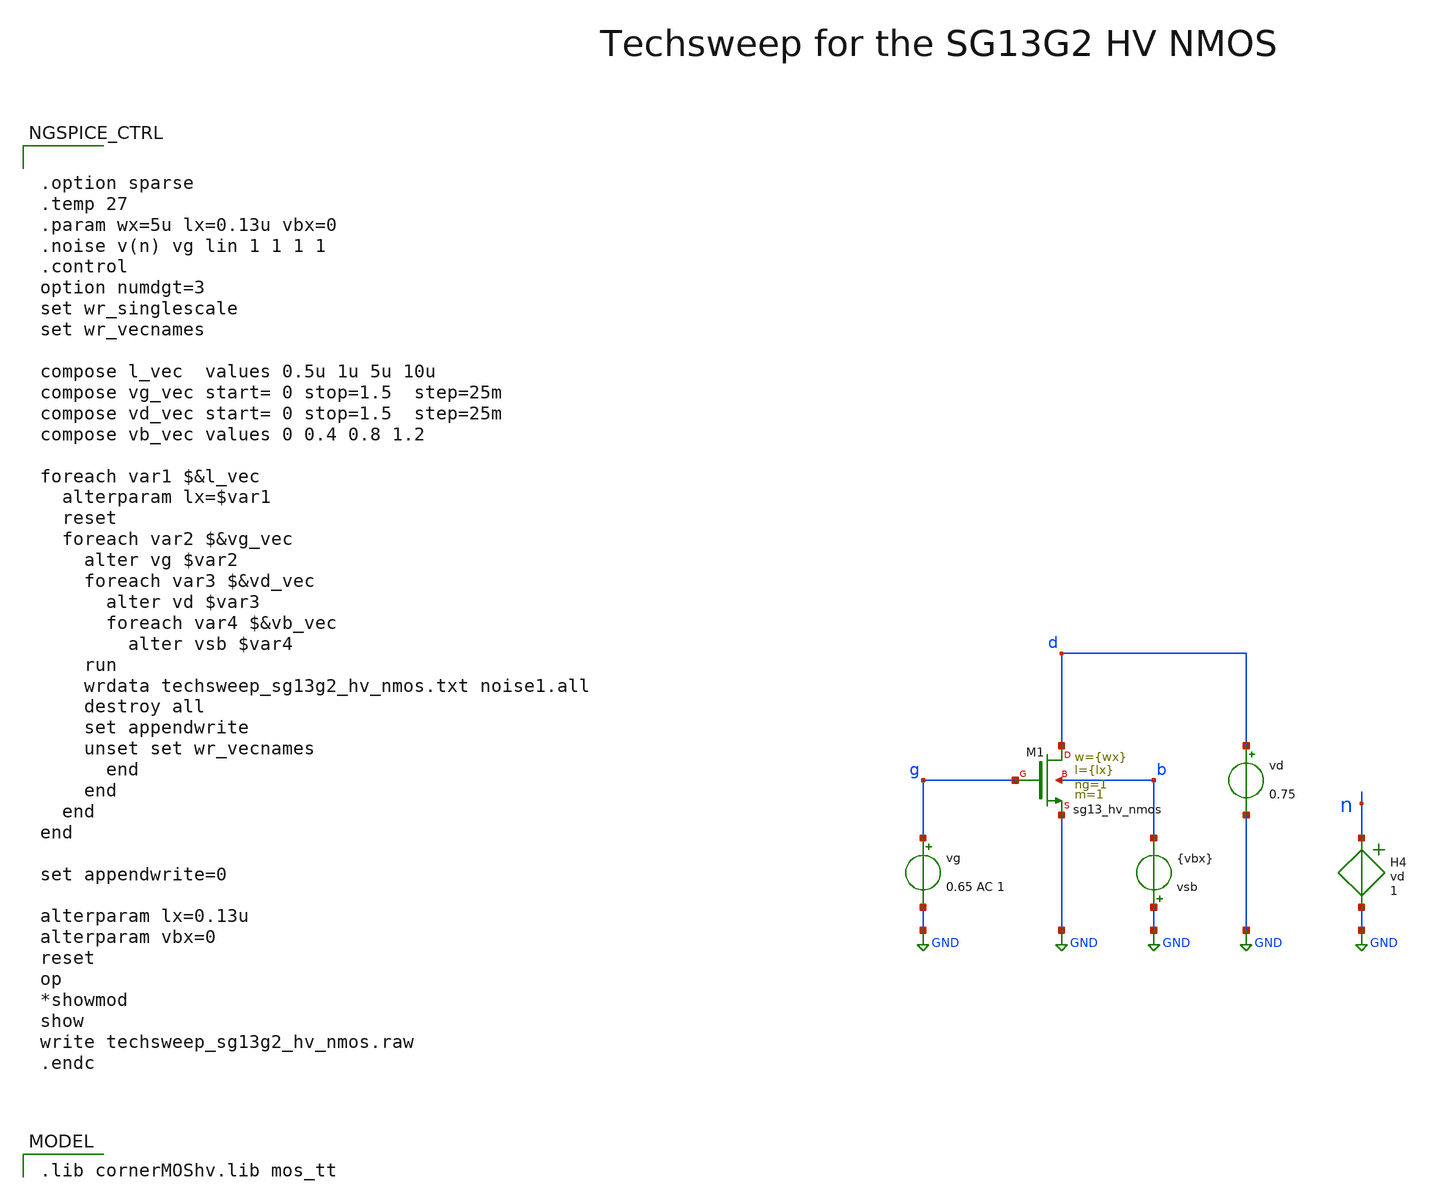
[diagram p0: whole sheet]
** sch_path: SG13G2_ATBS-ADC-main/xschem/techsweep/sg13g2_hv_nmos/techsweep_sg13g2_hv_nmos.sch
* (c) 2024 H. Pretl & S. Dorrer (adapted from B. Murmann)
**.subckt techsweep_sg13g2_hv_nmos
vg g GND 0.65 AC 1
vd d GND 0.75
vsb GND b {vbx}
H4 n GND vd 1
XM1 d g GND b sg13_hv_nmos w={wx} l={lx} ng=1 m=1 mm_ok=1
**** begin user architecture code
 .lib cornerMOShv.lib mos_tt



.option sparse
.temp 27
.param wx=5u lx=0.13u vbx=0
.noise v(n) vg lin 1 1 1 1
.control
option numdgt=3
set wr_singlescale
set wr_vecnames

compose l_vec  values 0.5u 1u 5u 10u
compose vg_vec start= 0 stop=1.5  step=25m
compose vd_vec start= 0 stop=1.5  step=25m
compose vb_vec values 0 0.4 0.8 1.2

foreach var1 $&l_vec
  alterparam lx=$var1
  reset
  foreach var2 $&vg_vec
    alter vg $var2
    foreach var3 $&vd_vec
      alter vd $var3
      foreach var4 $&vb_vec
        alter vsb $var4
	run
	wrdata techsweep_sg13g2_hv_nmos.txt noise1.all
	destroy all
	set appendwrite
	unset set wr_vecnames
      end
    end
  end
end

set appendwrite=0

alterparam lx=0.13u
alterparam vbx=0
reset
op
*showmod
show
write techsweep_sg13g2_hv_nmos.raw
.endc




.save b d g n
.save @n.xm1.nsg13_hv_nmos[cgsol]
.save @n.xm1.nsg13_hv_nmos[cgdol]
.save @n.xm1.nsg13_hv_nmos[cdd]
.save @n.xm1.nsg13_hv_nmos[cgb]
.save @n.xm1.nsg13_hv_nmos[cgd]
.save @n.xm1.nsg13_hv_nmos[cgg]
.save @n.xm1.nsg13_hv_nmos[cgs]
.save @n.xm1.nsg13_hv_nmos[css]
.save @n.xm1.nsg13_hv_nmos[gds]
.save @n.xm1.nsg13_hv_nmos[gm]
.save @n.xm1.nsg13_hv_nmos[gmb]
.save @n.xm1.nsg13_hv_nmos[ids]
.save @n.xm1.nsg13_hv_nmos[l]
.save @n.xm1.nsg13_hv_nmos[vgs]
.save @n.xm1.nsg13_hv_nmos[vds]
.save @n.xm1.nsg13_hv_nmos[vsb]
.save @n.xm1.nsg13_hv_nmos[vth]
.save @n.xm1.nsg13_hv_nmos[vdss]
.save @n.xm1.nsg13_hv_nmos[fug]
.save @n.xm1.nsg13_hv_nmos[sid]
.save @n.xm1.nsg13_hv_nmos[sfl]
.save @n.xm1.nsg13_hv_nmos[cjd]
.save @n.xm1.nsg13_hv_nmos[cjs]
.save @n.xm1.nsg13_hv_nmos[rg]


**** end user architecture code
**.ends
.GLOBAL GND
.end
